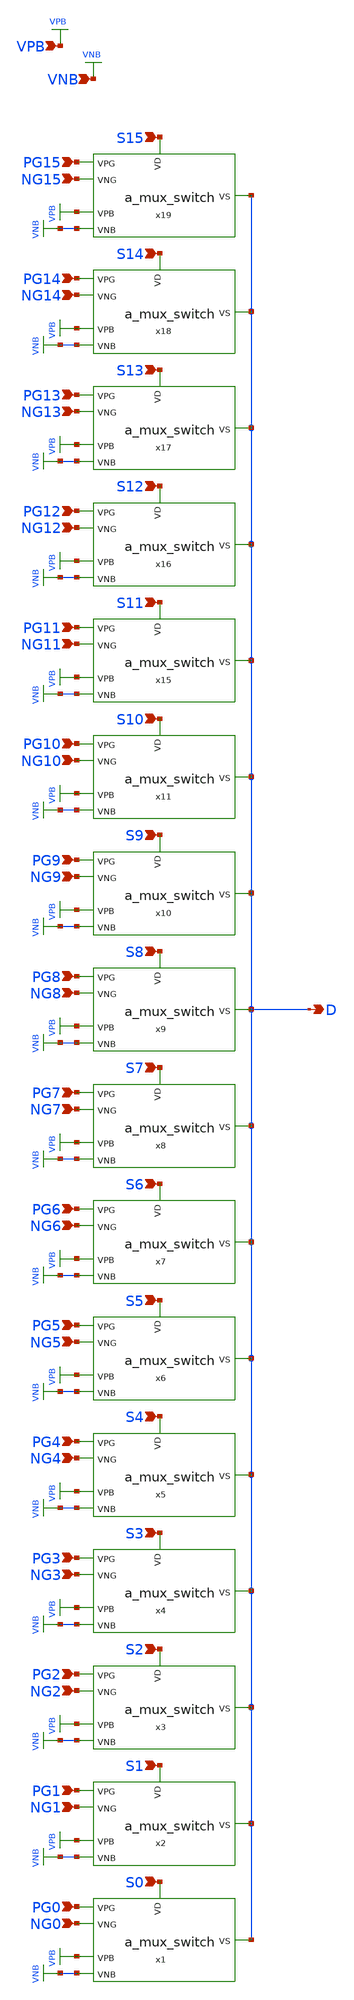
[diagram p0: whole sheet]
** sch_path: SP23_Tapeout/C2S2_Analog_TestChip-main/xschem/switch_x16.sch
**.subckt switch_x16 PG0 NG0 S0 PG1 NG1 S1 PG2 NG2 S2 PG3 NG3 S3 PG4 NG4 S4 PG5 NG5 S5 PG6 NG6 S6
*+ PG7 NG7 S7 PG8 NG8 S8 PG9 NG9 S9 PG10 NG10 S10 PG11 NG11 S11 PG12 NG12 S12 PG13 NG13 S13 PG14 NG14 S14
*+ PG15 NG15 S15 D VPB VNB
*.ipin PG0
*.ipin NG0
*.ipin S0
*.ipin PG1
*.ipin NG1
*.ipin S1
*.ipin PG2
*.ipin NG2
*.ipin S2
*.ipin PG3
*.ipin NG3
*.ipin S3
*.ipin PG4
*.ipin NG4
*.ipin S4
*.ipin PG5
*.ipin NG5
*.ipin S5
*.ipin PG6
*.ipin NG6
*.ipin S6
*.ipin PG7
*.ipin NG7
*.ipin S7
*.ipin PG8
*.ipin NG8
*.ipin S8
*.ipin PG9
*.ipin NG9
*.ipin S9
*.ipin PG10
*.ipin NG10
*.ipin S10
*.ipin PG11
*.ipin NG11
*.ipin S11
*.ipin PG12
*.ipin NG12
*.ipin S12
*.ipin PG13
*.ipin NG13
*.ipin S13
*.ipin PG14
*.ipin NG14
*.ipin S14
*.ipin PG15
*.ipin NG15
*.ipin S15
*.opin D
*.ipin VPB
*.ipin VNB
x1 S0 VNB NG0 VPB PG0 D a_mux_switch
x2 S1 VNB NG1 VPB PG1 D a_mux_switch
x3 S2 VNB NG2 VPB PG2 D a_mux_switch
x4 S3 VNB NG3 VPB PG3 D a_mux_switch
x5 S4 VNB NG4 VPB PG4 D a_mux_switch
x6 S5 VNB NG5 VPB PG5 D a_mux_switch
x7 S6 VNB NG6 VPB PG6 D a_mux_switch
x8 S7 VNB NG7 VPB PG7 D a_mux_switch
x9 S8 VNB NG8 VPB PG8 D a_mux_switch
x10 S9 VNB NG9 VPB PG9 D a_mux_switch
x11 S10 VNB NG10 VPB PG10 D a_mux_switch
x15 S11 VNB NG11 VPB PG11 D a_mux_switch
x16 S12 VNB NG12 VPB PG12 D a_mux_switch
x17 S13 VNB NG13 VPB PG13 D a_mux_switch
x18 S14 VNB NG14 VPB PG14 D a_mux_switch
x19 S15 VNB NG15 VPB PG15 D a_mux_switch
**.ends

* expanding   symbol:  a_mux_switch.sym # of pins=6
** sym_path: SP23_Tapeout/C2S2_Analog_TestChip-main/xschem/a_mux_switch.sym
** sch_path: SP23_Tapeout/C2S2_Analog_TestChip-main/xschem/a_mux_switch.sch
.subckt a_mux_switch VD VNB VNG VPB VPG VS
*.ipin VPG
*.ipin VNG
*.ipin VD
*.opin VS
*.ipin VPB
*.ipin VNB
XM1 VD VPG VS VPB sky130_fd_pr__pfet_01v8 L=0.15 W=95 nf=19 ad='int((nf+1)/2) * W/nf * 0.29' as='int((nf+2)/2) * W/nf * 0.29'
+ pd='2*int((nf+1)/2) * (W/nf + 0.29)' ps='2*int((nf+2)/2) * (W/nf + 0.29)' nrd='0.29 / W' nrs='0.29 / W'
+ sa=0 sb=0 sd=0 mult=1 m=1
XM2 VD VNG VS VNB sky130_fd_pr__nfet_01v8 L=0.15 W=45 nf=9 ad='int((nf+1)/2) * W/nf * 0.29' as='int((nf+2)/2) * W/nf * 0.29'
+ pd='2*int((nf+1)/2) * (W/nf + 0.29)' ps='2*int((nf+2)/2) * (W/nf + 0.29)' nrd='0.29 / W' nrs='0.29 / W'
+ sa=0 sb=0 sd=0 mult=1 m=1
.ends

.GLOBAL VPB
.GLOBAL VNB
.end
